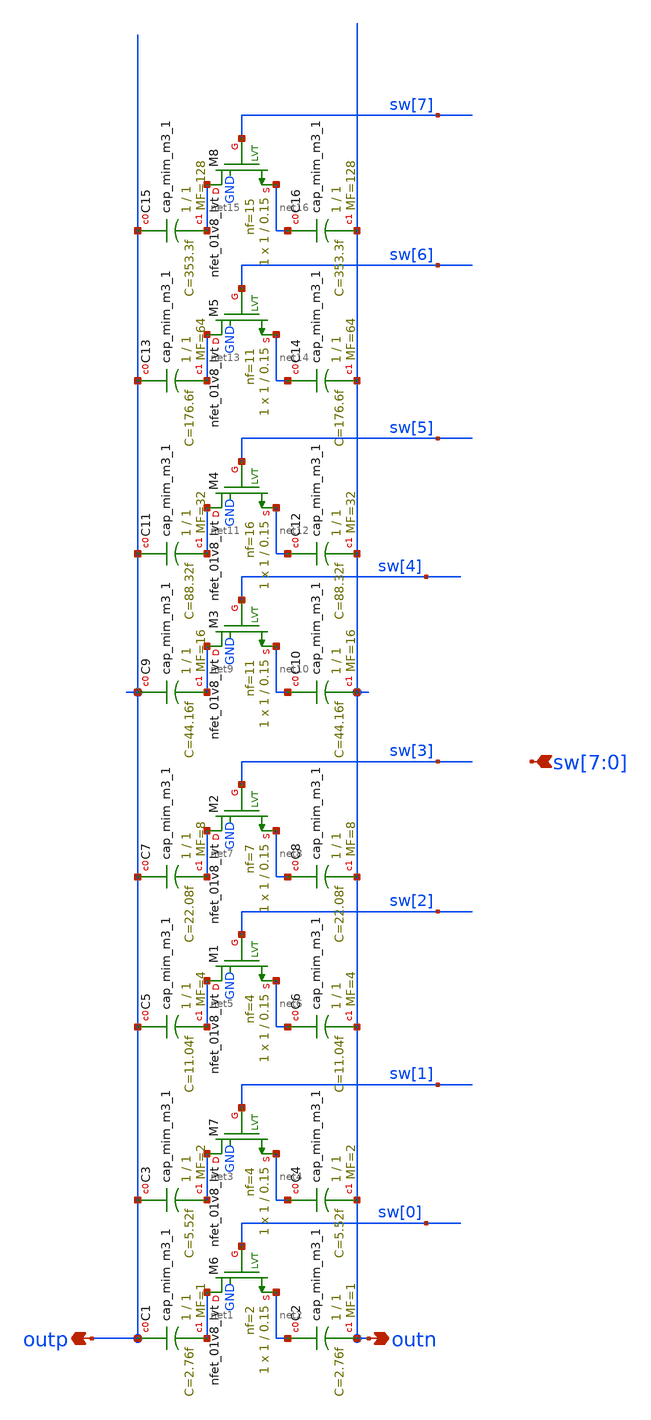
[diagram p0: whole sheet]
** sch_path: generators/lc-dco/xschem_rundir/mim_1m2C.sch
**.subckt mim_1m2C outn outp sw[7],sw[6],sw[5],sw[4],sw[3],sw[2],sw[1],sw[0]
*.opin outn
*.opin outp
*.ipin sw[7],sw[6],sw[5],sw[4],sw[3],sw[2],sw[1],sw[0]
XC1 outp net1 sky130_fd_pr__cap_mim_m3_1 W=1 L=1 MF=1 m=1
XC2 net2 outn sky130_fd_pr__cap_mim_m3_1 W=1 L=1 MF=1 m=1
XM6 net1 sw[0] net2 GND sky130_fd_pr__nfet_01v8_lvt L=0.15 W=1 nf=2 ad='int((nf+1)/2) * W/nf * 0.29'
+ as='int((nf+2)/2) * W/nf * 0.29' pd='2*int((nf+1)/2) * (W/nf + 0.29)' ps='2*int((nf+2)/2) * (W/nf + 0.29)'
+ nrd='0.29 / W' nrs='0.29 / W' sa=0 sb=0 sd=0 mult=1 m=1
XC3 outp net3 sky130_fd_pr__cap_mim_m3_1 W=1 L=1 MF=2 m=2
XC4 net4 outn sky130_fd_pr__cap_mim_m3_1 W=1 L=1 MF=2 m=2
XM7 net3 sw[1] net4 GND sky130_fd_pr__nfet_01v8_lvt L=0.15 W=1 nf=4 ad='int((nf+1)/2) * W/nf * 0.29'
+ as='int((nf+2)/2) * W/nf * 0.29' pd='2*int((nf+1)/2) * (W/nf + 0.29)' ps='2*int((nf+2)/2) * (W/nf + 0.29)'
+ nrd='0.29 / W' nrs='0.29 / W' sa=0 sb=0 sd=0 mult=1 m=1
XC5 outp net5 sky130_fd_pr__cap_mim_m3_1 W=1 L=1 MF=4 m=4
XC6 net6 outn sky130_fd_pr__cap_mim_m3_1 W=1 L=1 MF=4 m=4
XM1 net5 sw[2] net6 GND sky130_fd_pr__nfet_01v8_lvt L=0.15 W=1 nf=4 ad='int((nf+1)/2) * W/nf * 0.29'
+ as='int((nf+2)/2) * W/nf * 0.29' pd='2*int((nf+1)/2) * (W/nf + 0.29)' ps='2*int((nf+2)/2) * (W/nf + 0.29)'
+ nrd='0.29 / W' nrs='0.29 / W' sa=0 sb=0 sd=0 mult=1 m=1
XC7 outp net7 sky130_fd_pr__cap_mim_m3_1 W=1 L=1 MF=8 m=8
XC8 net8 outn sky130_fd_pr__cap_mim_m3_1 W=1 L=1 MF=8 m=8
XM2 net7 sw[3] net8 GND sky130_fd_pr__nfet_01v8_lvt L=0.15 W=1 nf=7 ad='int((nf+1)/2) * W/nf * 0.29'
+ as='int((nf+2)/2) * W/nf * 0.29' pd='2*int((nf+1)/2) * (W/nf + 0.29)' ps='2*int((nf+2)/2) * (W/nf + 0.29)'
+ nrd='0.29 / W' nrs='0.29 / W' sa=0 sb=0 sd=0 mult=1 m=1
XC9 outp net9 sky130_fd_pr__cap_mim_m3_1 W=1 L=1 MF=16 m=16
XC10 net10 outn sky130_fd_pr__cap_mim_m3_1 W=1 L=1 MF=16 m=16
XM3 net9 sw[4] net10 GND sky130_fd_pr__nfet_01v8_lvt L=0.15 W=1 nf=11 ad='int((nf+1)/2) * W/nf * 0.29'
+ as='int((nf+2)/2) * W/nf * 0.29' pd='2*int((nf+1)/2) * (W/nf + 0.29)' ps='2*int((nf+2)/2) * (W/nf + 0.29)'
+ nrd='0.29 / W' nrs='0.29 / W' sa=0 sb=0 sd=0 mult=1 m=1
XC11 outp net11 sky130_fd_pr__cap_mim_m3_1 W=1 L=1 MF=32 m=32
XC12 net12 outn sky130_fd_pr__cap_mim_m3_1 W=1 L=1 MF=32 m=32
XM4 net11 sw[5] net12 GND sky130_fd_pr__nfet_01v8_lvt L=0.15 W=1 nf=16 ad='int((nf+1)/2) * W/nf * 0.29'
+ as='int((nf+2)/2) * W/nf * 0.29' pd='2*int((nf+1)/2) * (W/nf + 0.29)' ps='2*int((nf+2)/2) * (W/nf + 0.29)'
+ nrd='0.29 / W' nrs='0.29 / W' sa=0 sb=0 sd=0 mult=1 m=1
XC13 outp net13 sky130_fd_pr__cap_mim_m3_1 W=1 L=1 MF=64 m=64
XC14 net14 outn sky130_fd_pr__cap_mim_m3_1 W=1 L=1 MF=64 m=64
XM5 net13 sw[6] net14 GND sky130_fd_pr__nfet_01v8_lvt L=0.15 W=1 nf=11 ad='int((nf+1)/2) * W/nf * 0.29'
+ as='int((nf+2)/2) * W/nf * 0.29' pd='2*int((nf+1)/2) * (W/nf + 0.29)' ps='2*int((nf+2)/2) * (W/nf + 0.29)'
+ nrd='0.29 / W' nrs='0.29 / W' sa=0 sb=0 sd=0 mult=1 m=1
XC15 outp net15 sky130_fd_pr__cap_mim_m3_1 W=1 L=1 MF=128 m=128
XC16 net16 outn sky130_fd_pr__cap_mim_m3_1 W=1 L=1 MF=128 m=128
XM8 net15 sw[7] net16 GND sky130_fd_pr__nfet_01v8_lvt L=0.15 W=1 nf=15 ad='int((nf+1)/2) * W/nf * 0.29'
+ as='int((nf+2)/2) * W/nf * 0.29' pd='2*int((nf+1)/2) * (W/nf + 0.29)' ps='2*int((nf+2)/2) * (W/nf + 0.29)'
+ nrd='0.29 / W' nrs='0.29 / W' sa=0 sb=0 sd=0 mult=1 m=1
**.ends
.end
